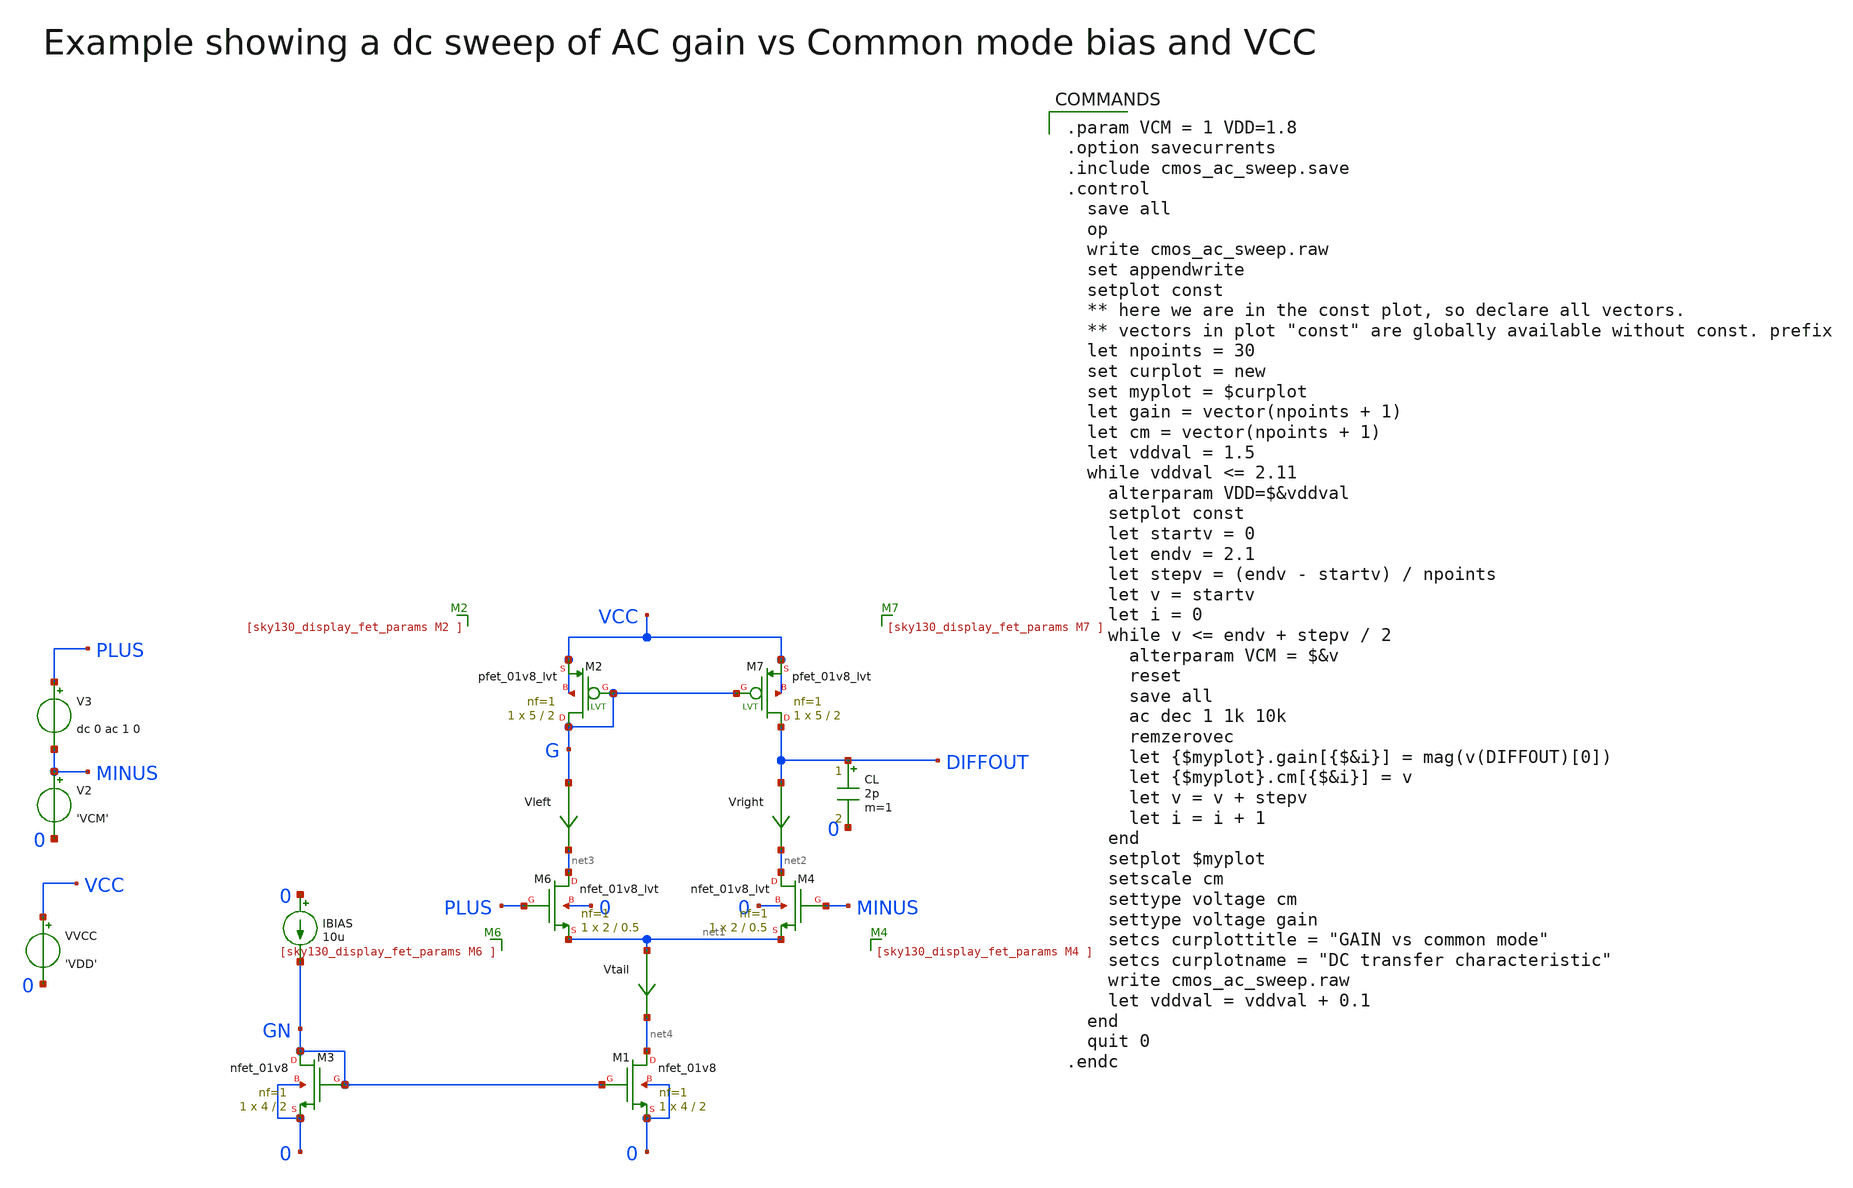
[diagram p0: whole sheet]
** sch_path: sky130A/xschem_libs/sky130_tests/cmos_ac_sweep/schematic/cmos_ac_sweep.sch
* Copyright 2021 Stefan Frederik Schippers
* Licensed under the Apache License, Version 2.0 (the "License");
* you may not use this file except in compliance with the License.
* You may obtain a copy of the License at
* https://www.apache.org/licenses/LICENSE-2.0
* Unless required by applicable law or agreed to in writing, software
* distributed under the License is distributed on an "AS IS" BASIS,
* WITHOUT WARRANTIES OR CONDITIONS OF ANY KIND, either express or implied.
* See the License for the specific language governing permissions and
* limitations under the License.
**.subckt cmos_ac_sweep
VVCC VCC 0 'VDD'
IBIAS 0 GN 10u
CL DIFFOUT 0 2p m=1
Vright DIFFOUT net2 0
.save i(vright)
V3 PLUS MINUS dc 0 ac 1 0
V2 MINUS 0 'VCM'
XM7 DIFFOUT G VCC VCC sky130_fd_pr__pfet_01v8_lvt L=2 W=5 nf=1 ad='int((1 + 1)/2) * 5 / 1 * 0.29' as='int((1 + 2)/2) * 5 / 1 * 0.29'
+ pd='2*int((1 + 1)/2) * (5 / 1 + 0.29)' ps='2*int((1 + 2)/2) * (5 / 1 + 0.29)' nrd='0.29 / 5 ' nrs='0.29 / 5 '
+ sa=0 sb=0 sd=0 mult=1 m=1
XM2 G G VCC VCC sky130_fd_pr__pfet_01v8_lvt L=2 W=5 nf=1 ad='int((1 + 1)/2) * 5 / 1 * 0.29' as='int((1 + 2)/2) * 5 / 1 * 0.29'
+ pd='2*int((1 + 1)/2) * (5 / 1 + 0.29)' ps='2*int((1 + 2)/2) * (5 / 1 + 0.29)' nrd='0.29 / 5 ' nrs='0.29 / 5 '
+ sa=0 sb=0 sd=0 mult=1 m=1
XM6 net3 PLUS net1 0 sky130_fd_pr__nfet_01v8_lvt L=0.5 W=2 nf=1 ad='int((1 + 1)/2) * 2 / 1 * 0.29' as='int((1 + 2)/2) * 2 / 1 * 0.29'
+ pd='2*int((1 + 1)/2) * (2 / 1 + 0.29)' ps='2*int((1 + 2)/2) * (2 / 1 + 0.29)' nrd='0.29 / 2 ' nrs='0.29 / 2 '
+ sa=0 sb=0 sd=0 mult=1 m=1
XM4 net2 MINUS net1 0 sky130_fd_pr__nfet_01v8_lvt L=0.5 W=2 nf=1 ad='int((1 + 1)/2) * 2 / 1 * 0.29' as='int((1 + 2)/2) * 2 / 1 * 0.29'
+ pd='2*int((1 + 1)/2) * (2 / 1 + 0.29)' ps='2*int((1 + 2)/2) * (2 / 1 + 0.29)' nrd='0.29 / 2 ' nrs='0.29 / 2 '
+ sa=0 sb=0 sd=0 mult=1 m=1
XM1 net4 GN 0 0 sky130_fd_pr__nfet_01v8 L=2 W=4 nf=1 ad='int((1 + 1)/2) * 4 / 1 * 0.29' as='int((1 + 2)/2) * 4 / 1 * 0.29'
+ pd='2*int((1 + 1)/2) * (4 / 1 + 0.29)' ps='2*int((1 + 2)/2) * (4 / 1 + 0.29)' nrd='0.29 / 4 ' nrs='0.29 / 4 '
+ sa=0 sb=0 sd=0 mult=1 m=1
XM3 GN GN 0 0 sky130_fd_pr__nfet_01v8 L=2 W=4 nf=1 ad='int((1 + 1)/2) * 4 / 1 * 0.29' as='int((1 + 2)/2) * 4 / 1 * 0.29'
+ pd='2*int((1 + 1)/2) * (4 / 1 + 0.29)' ps='2*int((1 + 2)/2) * (4 / 1 + 0.29)' nrd='0.29 / 4 ' nrs='0.29 / 4 '
+ sa=0 sb=0 sd=0 mult=1 m=1
Vtail net1 net4 0
.save i(vtail)
Vleft G net3 0
.save i(vleft)
**** begin user architecture code

.param VCM = 1 VDD=1.8
.option savecurrents
.include cmos_ac_sweep.save
.control
  save all
  op
  write cmos_ac_sweep.raw
  set appendwrite
  setplot const
  ** here we are in the const plot, so declare all vectors.
  ** vectors in plot "const" are globally available without const. prefix
  let npoints = 30
  set curplot = new
  set myplot = $curplot
  let gain = vector(npoints + 1)
  let cm = vector(npoints + 1)
  let vddval = 1.5
  while vddval <= 2.11
    alterparam VDD=$&vddval
    setplot const
    let startv = 0
    let endv = 2.1
    let stepv = (endv - startv) / npoints
    let v = startv
    let i = 0
    while v <= endv + stepv / 2
      alterparam VCM = $&v
      reset
      save all
      ac dec 1 1k 10k
      remzerovec
      let {$myplot}.gain[{$&i}] = mag(v(DIFFOUT)[0])
      let {$myplot}.cm[{$&i}] = v
      let v = v + stepv
      let i = i + 1
    end
    setplot $myplot
    setscale cm
    settype voltage cm
    settype voltage gain
    setcs curplottitle = "GAIN vs common mode"
    setcs curplotname = "DC transfer characteristic"
    write cmos_ac_sweep.raw
    let vddval = vddval + 0.1
  end
  quit 0
.endc



** opencircuitdesign pdks install
.lib $::SKYWATER_MODELS/sky130.lib.spice tt

**** end user architecture code
**.ends
.end
